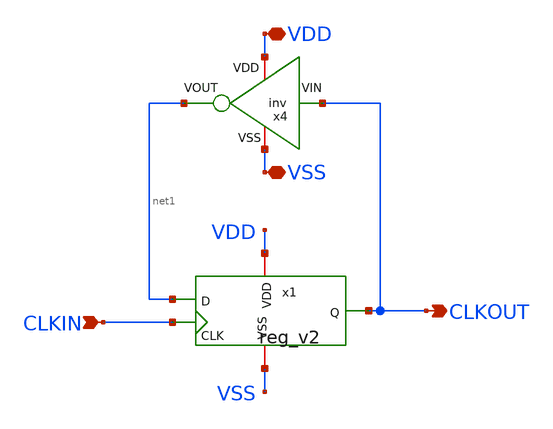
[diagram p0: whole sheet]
** sch_path: Custom_std_cells/div_freq_x2.sch
**.subckt div_freq_x2 VDD VSS CLKIN CLKOUT
*.iopin VDD
*.iopin VSS
*.ipin CLKIN
*.opin CLKOUT
x1 VDD CLKIN VSS CLKOUT net1 reg_v2
x4 VDD net1 CLKOUT VSS inv
**.ends

* expanding   symbol:  /foss/designs/PhaseInterpolator/Custom_std_Cells/reg_v2.sym # of pins=5
** sym_path: /foss/designs/PhaseInterpolator/Custom_std_Cells/reg_v2.sym
** sch_path: /foss/designs/PhaseInterpolator/Custom_std_Cells/reg_v2.sch
.subckt reg_v2 VDD CLK VSS Q D
*.iopin VDD
*.iopin VSS
*.ipin CLK
*.ipin D
*.opin Q
x3 net7 CLK CLK_B net2 VDD VSS tg_custom
x9 VDD CLK_B CLK VSS inv
x4 VDD net2 net1 VSS inv
x8 VDD net4 D VSS inv
x11 VDD net3 Q VSS inv
x10 VDD net5 net1 VSS inv
x2 net7 CLK_B CLK net4 VDD VSS tg_custom
x6 net6 CLK_B CLK net3 VDD VSS tg_custom
x7 net6 CLK CLK_B net5 VDD VSS tg_custom
x5 VDD net1 net7 VSS inv
x1 VDD Q net6 VSS inv
.ends


* expanding   symbol:  /foss/designs/PhaseInterpolator/Custom_std_Cells/tg_custom.sym # of pins=6
** sym_path: /foss/designs/PhaseInterpolator/Custom_std_Cells/tg_custom.sym
** sch_path: /foss/designs/PhaseInterpolator/Custom_std_Cells/tg_custom.sch
.subckt tg_custom VOUT VSN VSP VIN VBP VBN
*.iopin VIN
*.iopin VSN
*.iopin VOUT
*.iopin VSP
*.iopin VBN
*.iopin VBP
XM1 VOUT VSN VIN VBN sg13_lv_nmos w=0.15u l=0.13u ng=1 m=1 mm_ok=1
XM2 VOUT VSP VIN VBP sg13_lv_pmos w=0.15u l=0.13u ng=1 m=2 mm_ok=1
.ends

.end
